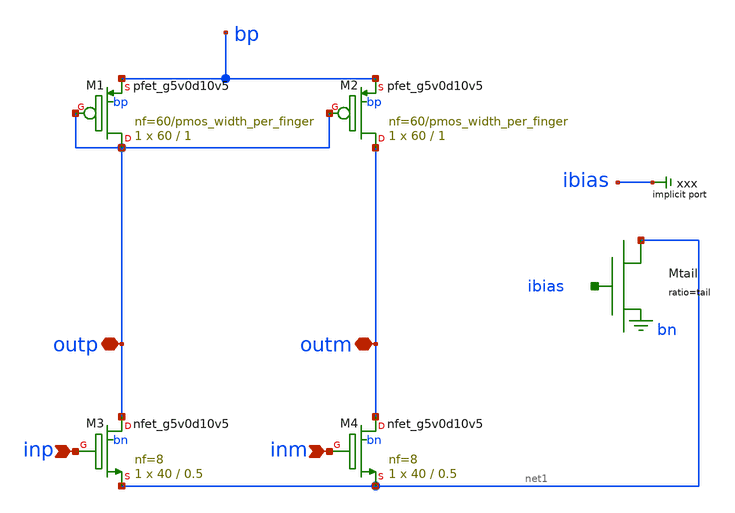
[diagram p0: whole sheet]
** sch_path: xschem/mosbius_lib/mosbius_ota.sch
**.subckt mosbius_ota inp inm outp outm
*.ipin inp
*.ipin inm
*.iopin outp
*.iopin outm
XM3 outp inp net1 bn sky130_fd_pr__nfet_g5v0d10v5 L=0.5 W=40 nf=8 ad='int((nf+1)/2) * W/nf * 0.29' as='int((nf+2)/2) * W/nf * 0.29'
+ pd='2*int((nf+1)/2) * (W/nf + 0.29)' ps='2*int((nf+2)/2) * (W/nf + 0.29)' nrd='0.29 / W' nrs='0.29 / W'
+ sa=0 sb=0 sd=0 mult=1 m=1
XM4 outm inm net1 bn sky130_fd_pr__nfet_g5v0d10v5 L=0.5 W=40 nf=8 ad='int((nf+1)/2) * W/nf * 0.29' as='int((nf+2)/2) * W/nf * 0.29'
+ pd='2*int((nf+1)/2) * (W/nf + 0.29)' ps='2*int((nf+2)/2) * (W/nf + 0.29)' nrd='0.29 / W' nrs='0.29 / W'
+ sa=0 sb=0 sd=0 mult=1 m=1
XM1 outp outp bp bp sky130_fd_pr__pfet_g5v0d10v5 L=1 W=60 nf=60/pmos_width_per_finger ad='int((nf+1)/2) * W/nf * 0.29'
+ as='int((nf+2)/2) * W/nf * 0.29' pd='2*int((nf+1)/2) * (W/nf + 0.29)' ps='2*int((nf+2)/2) * (W/nf + 0.29)'
+ nrd='0.29 / W' nrs='0.29 / W' sa=0 sb=0 sd=0 mult=1 m=1
XM2 outm outp bp bp sky130_fd_pr__pfet_g5v0d10v5 L=1 W=60 nf=60/pmos_width_per_finger ad='int((nf+1)/2) * W/nf * 0.29'
+ as='int((nf+2)/2) * W/nf * 0.29' pd='2*int((nf+1)/2) * (W/nf + 0.29)' ps='2*int((nf+2)/2) * (W/nf + 0.29)'
+ nrd='0.29 / W' nrs='0.29 / W' sa=0 sb=0 sd=0 mult=1 m=1
XMtail net1 ibias bn mosbius_nsink ratio=tail
* implicit port xxx
**.ends

* expanding   symbol:  mosbius_nsink.sym # of pins=1
** sym_path: xschem/mosbius_lib/mosbius_nsink.sym
** sch_path: xschem/mosbius_lib/mosbius_nsink.sch
.subckt mosbius_nsink out ibias b  ratio=1
*.iopin ibias
*.iopin b
*.iopin out
XM1 ibias ibias b b sky130_fd_pr__nfet_g5v0d10v5 L=1 W=10 nf=2 ad='int((nf+1)/2) * W/nf * 0.29' as='int((nf+2)/2) * W/nf * 0.29'
+ pd='2*int((nf+1)/2) * (W/nf + 0.29)' ps='2*int((nf+2)/2) * (W/nf + 0.29)' nrd='0.29 / W' nrs='0.29 / W'
+ sa=0 sb=0 sd=0 mult=1 m=1
XM2 out ibias b b sky130_fd_pr__nfet_g5v0d10v5 L=1 W=10*ratio nf=2*ratio ad='int((nf+1)/2) * W/nf * 0.29'
+ as='int((nf+2)/2) * W/nf * 0.29' pd='2*int((nf+1)/2) * (W/nf + 0.29)' ps='2*int((nf+2)/2) * (W/nf + 0.29)'
+ nrd='0.29 / W' nrs='0.29 / W' sa=0 sb=0 sd=0 mult=1 m=1
.ends

.end
